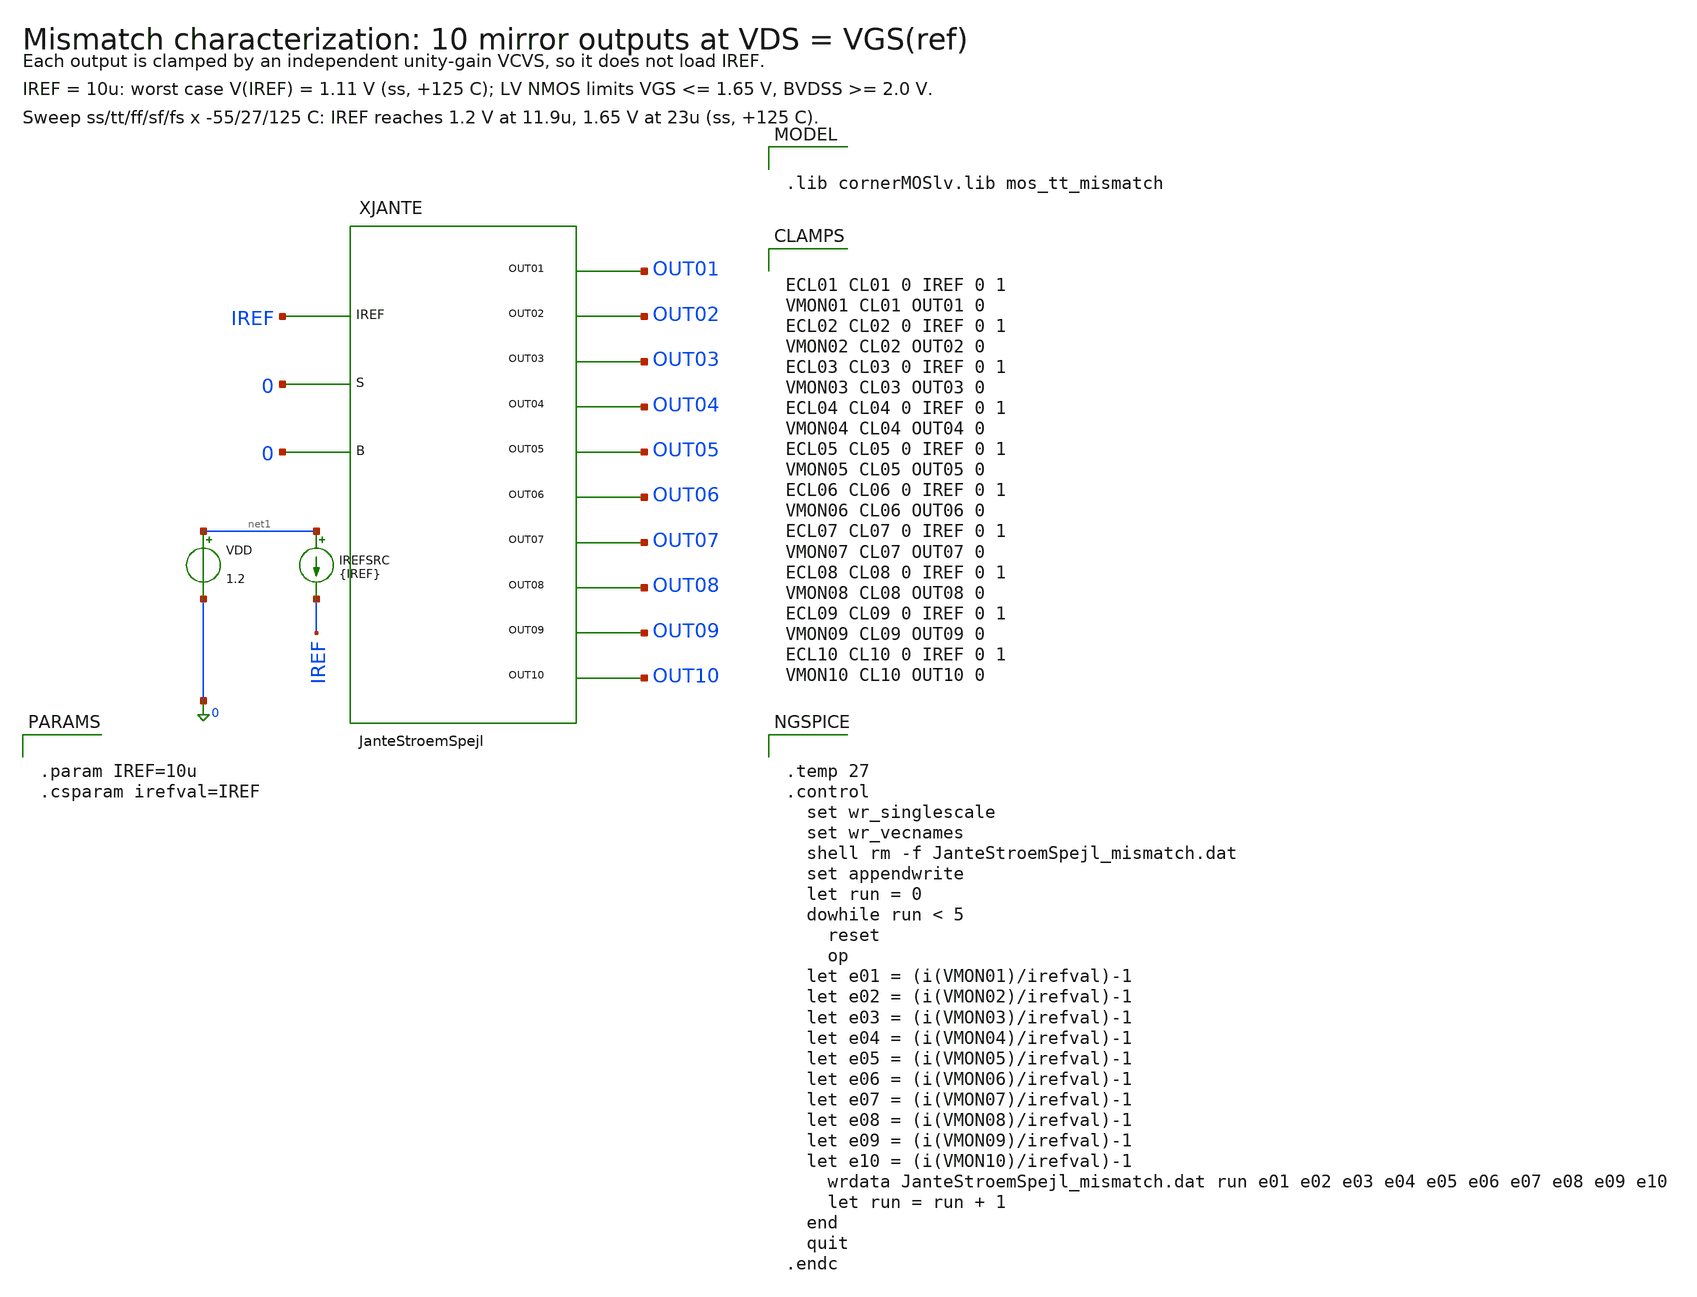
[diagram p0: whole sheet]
** sch_path: sudelbuecher/JanteStroemSpejl/JanteStroemSpejl_tb_mismatch.sch
**.subckt JanteStroemSpejl_tb_mismatch
XJANTE IREF 0 0 OUT01 OUT02 OUT03 OUT04 OUT05 OUT06 OUT07 OUT08 OUT09 OUT10 JanteStroemSpejl
VDD net1 0 1.2
IREFSRC net1 IREF {IREF}
**** begin user architecture code


.param IREF=10u
.csparam irefval=IREF



.lib cornerMOSlv.lib mos_tt_mismatch



ECL01 CL01 0 IREF 0 1
VMON01 CL01 OUT01 0
ECL02 CL02 0 IREF 0 1
VMON02 CL02 OUT02 0
ECL03 CL03 0 IREF 0 1
VMON03 CL03 OUT03 0
ECL04 CL04 0 IREF 0 1
VMON04 CL04 OUT04 0
ECL05 CL05 0 IREF 0 1
VMON05 CL05 OUT05 0
ECL06 CL06 0 IREF 0 1
VMON06 CL06 OUT06 0
ECL07 CL07 0 IREF 0 1
VMON07 CL07 OUT07 0
ECL08 CL08 0 IREF 0 1
VMON08 CL08 OUT08 0
ECL09 CL09 0 IREF 0 1
VMON09 CL09 OUT09 0
ECL10 CL10 0 IREF 0 1
VMON10 CL10 OUT10 0




.temp 27
.control
  set wr_singlescale
  set wr_vecnames
  shell rm -f JanteStroemSpejl_mismatch.dat
  set appendwrite
  let run = 0
  dowhile run < 5
    reset
    op
  let e01 = (i(VMON01)/irefval)-1
  let e02 = (i(VMON02)/irefval)-1
  let e03 = (i(VMON03)/irefval)-1
  let e04 = (i(VMON04)/irefval)-1
  let e05 = (i(VMON05)/irefval)-1
  let e06 = (i(VMON06)/irefval)-1
  let e07 = (i(VMON07)/irefval)-1
  let e08 = (i(VMON08)/irefval)-1
  let e09 = (i(VMON09)/irefval)-1
  let e10 = (i(VMON10)/irefval)-1
    wrdata JanteStroemSpejl_mismatch.dat run e01 e02 e03 e04 e05 e06 e07 e08 e09 e10
    let run = run + 1
  end
  quit
.endc


**** end user architecture code
**.ends

* expanding   symbol:  JanteStroemSpejl.sym # of pins=13
** sym_path: sudelbuecher/JanteStroemSpejl/JanteStroemSpejl_chat_export/ref/JanteStroemSpejl.sym
** sch_path: sudelbuecher/JanteStroemSpejl/JanteStroemSpejl_chat_export/ref/JanteStroemSpejl.sch
.subckt JanteStroemSpejl IREF S B OUT01 OUT02 OUT03 OUT04 OUT05 OUT06 OUT07 OUT08 OUT09 OUT10
*.iopin IREF
*.iopin S
*.iopin B
*.iopin OUT01
*.iopin OUT02
*.iopin OUT03
*.iopin OUT04
*.iopin OUT05
*.iopin OUT06
*.iopin OUT07
*.iopin OUT08
*.iopin OUT09
*.iopin OUT10
**** begin user architecture code


.param lambda=0.08u
.param WJ='4*lambda'
.param LJ='64*lambda'


**** end user architecture code
XM_L01 net1 net2 net3 net4 sg13_lv_nmos w=0.15u l={LJ ng=1 m=1 mm_ok=1
XM_R01 net5 net6 net7 net8 sg13_lv_nmos w=0.15u l={LJ ng=1 m=1 mm_ok=1
XM_L02 net9 net10 net11 net12 sg13_lv_nmos w=0.15u l={LJ ng=1 m=1 mm_ok=1
XM_R02 net13 net14 net15 net16 sg13_lv_nmos w=0.15u l={LJ ng=1 m=1 mm_ok=1
XM_L03 net17 net18 net19 net20 sg13_lv_nmos w=0.15u l={LJ ng=1 m=1 mm_ok=1
XM_R03 net21 net22 net23 net24 sg13_lv_nmos w=0.15u l={LJ ng=1 m=1 mm_ok=1
XM_L04 net25 net26 net27 net28 sg13_lv_nmos w=0.15u l={LJ ng=1 m=1 mm_ok=1
XM_R04 net29 net30 net31 net32 sg13_lv_nmos w=0.15u l={LJ ng=1 m=1 mm_ok=1
XM_L05 net33 net34 net35 net36 sg13_lv_nmos w=0.15u l={LJ ng=1 m=1 mm_ok=1
XM_R05 net37 net38 net39 net40 sg13_lv_nmos w=0.15u l={LJ ng=1 m=1 mm_ok=1
XM_L06 net41 net42 net43 net44 sg13_lv_nmos w=0.15u l={LJ ng=1 m=1 mm_ok=1
XM_R06 net45 net46 net47 net48 sg13_lv_nmos w=0.15u l={LJ ng=1 m=1 mm_ok=1
XM_L07 net49 net50 net51 net52 sg13_lv_nmos w=0.15u l={LJ ng=1 m=1 mm_ok=1
XM_R07 net53 net54 net55 net56 sg13_lv_nmos w=0.15u l={LJ ng=1 m=1 mm_ok=1
XM_L08 net57 net58 net59 net60 sg13_lv_nmos w=0.15u l={LJ ng=1 m=1 mm_ok=1
XM_R08 net61 net62 net63 net64 sg13_lv_nmos w=0.15u l={LJ ng=1 m=1 mm_ok=1
XM_L09 net65 net66 net67 net68 sg13_lv_nmos w=0.15u l={LJ ng=1 m=1 mm_ok=1
XM_R09 net69 net70 net71 net72 sg13_lv_nmos w=0.15u l={LJ ng=1 m=1 mm_ok=1
XM_L10 net73 net74 net75 net76 sg13_lv_nmos w=0.15u l={LJ ng=1 m=1 mm_ok=1
XM_R10 net77 net78 net79 net80 sg13_lv_nmos w=0.15u l={LJ ng=1 m=1 mm_ok=1
XM_L11 net81 net82 net83 net84 sg13_lv_nmos w=0.15u l={LJ ng=1 m=1 mm_ok=1
XM_R11 net85 net86 net87 net88 sg13_lv_nmos w=0.15u l={LJ ng=1 m=1 mm_ok=1
.ends

.end
